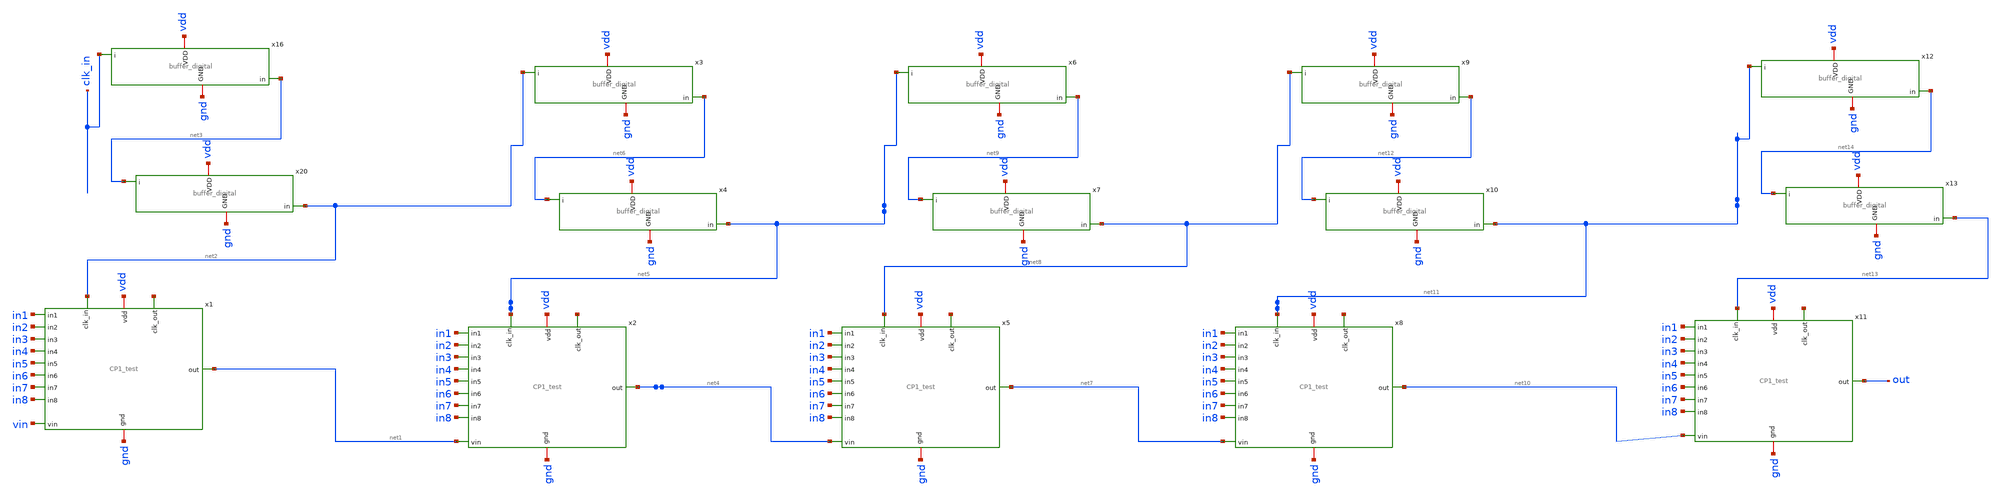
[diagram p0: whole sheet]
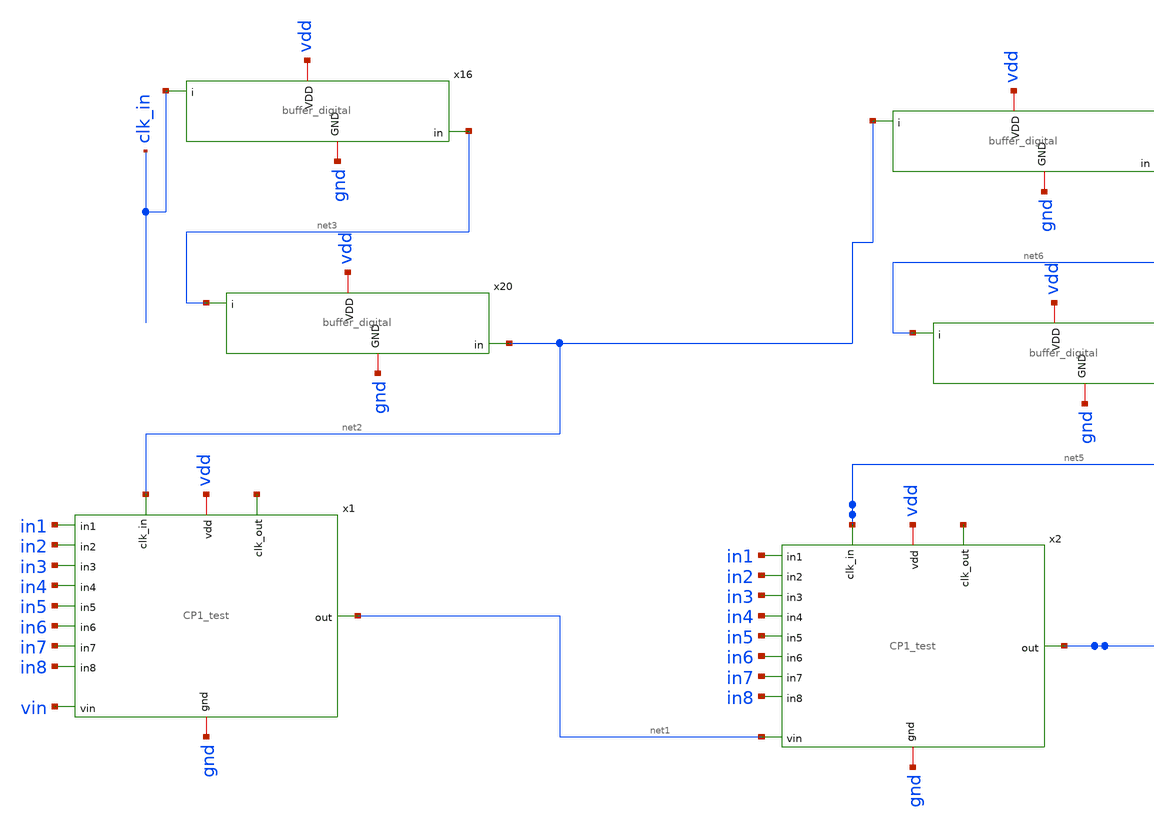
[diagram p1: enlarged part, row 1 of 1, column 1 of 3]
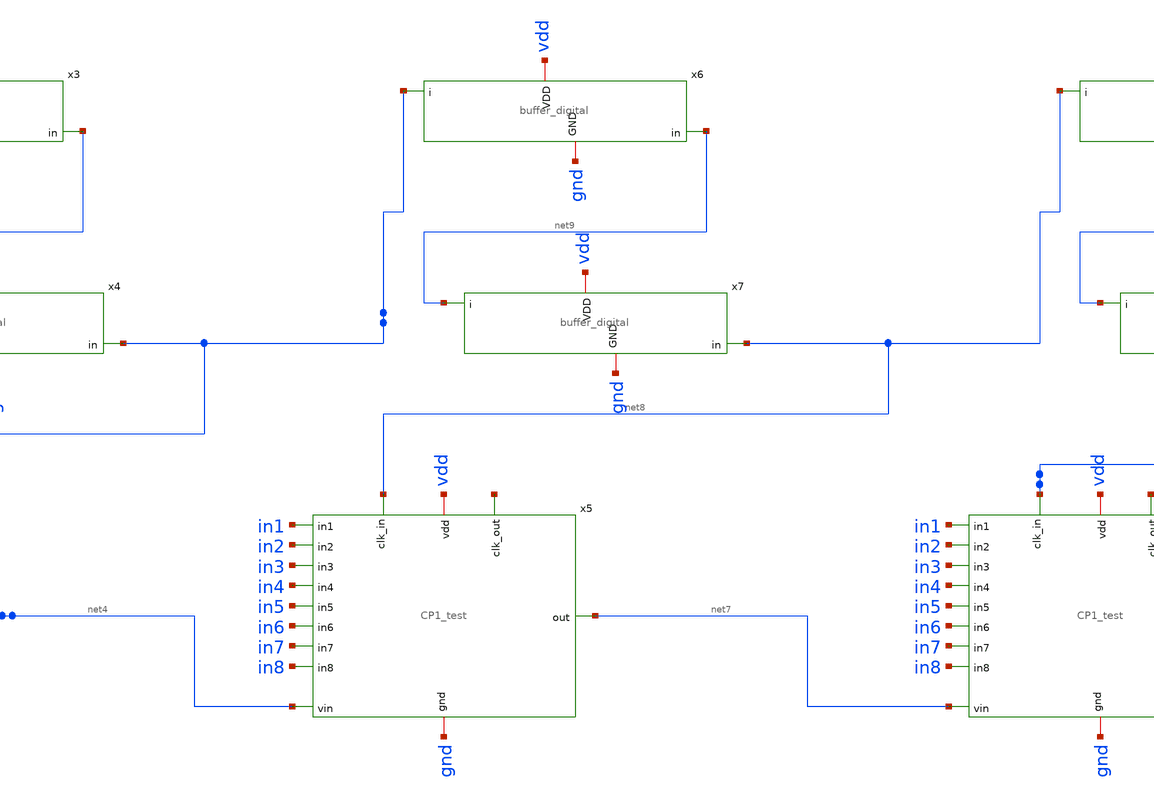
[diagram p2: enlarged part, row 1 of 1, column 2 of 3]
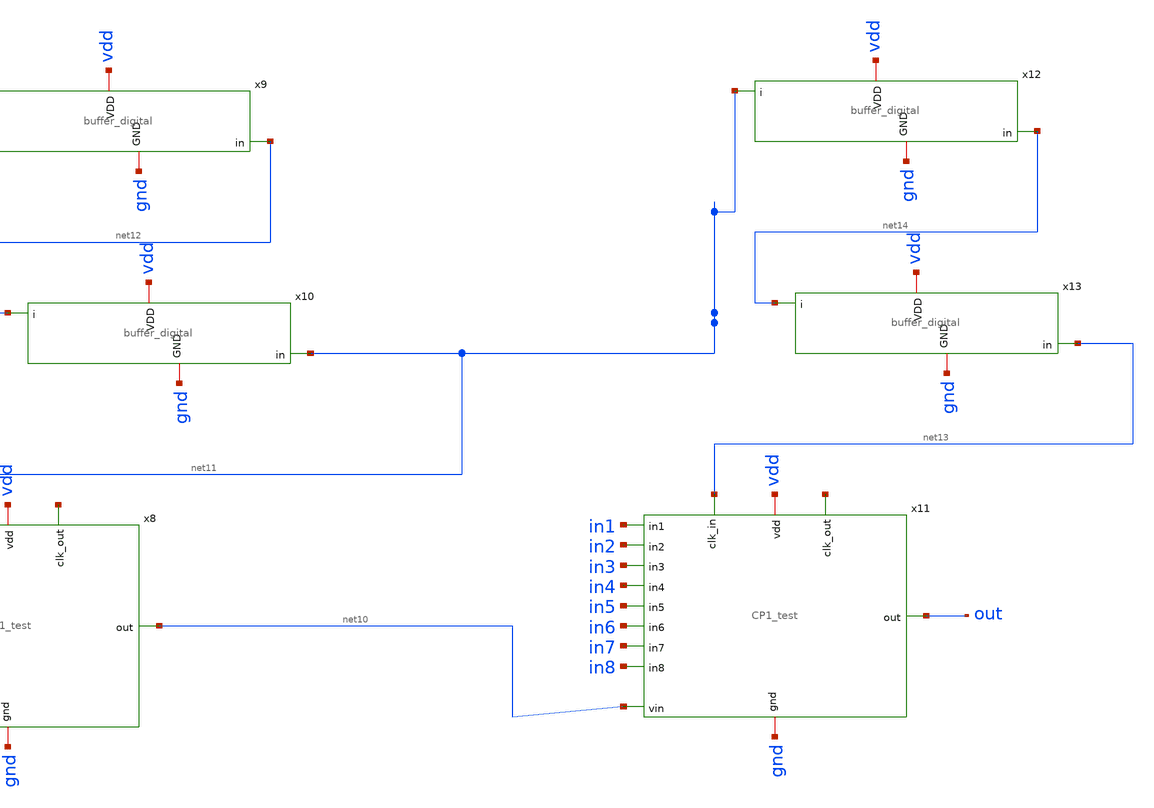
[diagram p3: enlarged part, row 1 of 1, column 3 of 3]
** sch_path: xschem/cp1_buffer_5stage_xschem.sch
**.subckt cp1_buffer_5stage_xschem
x1 gnd net2 vin net1 in1 in2 in3 in4 in5 in6 in7 in8 vdd net15 CP1_test
x16 gnd vdd clk_in net3 buffer_digital
x20 gnd vdd net3 net2 buffer_digital
x2 gnd net5 net1 net4 in1 in2 in3 in4 in5 in6 in7 in8 vdd net16 CP1_test
x3 gnd vdd net2 net6 buffer_digital
x4 gnd vdd net6 net5 buffer_digital
x5 gnd net8 net4 net7 in1 in2 in3 in4 in5 in6 in7 in8 vdd net17 CP1_test
x6 gnd vdd net5 net9 buffer_digital
x7 gnd vdd net9 net8 buffer_digital
x8 gnd net11 net7 net10 in1 in2 in3 in4 in5 in6 in7 in8 vdd net18 CP1_test
x9 gnd vdd net8 net12 buffer_digital
x10 gnd vdd net12 net11 buffer_digital
x11 gnd net13 net10 out in1 in2 in3 in4 in5 in6 in7 in8 vdd net19 CP1_test
x12 gnd vdd net11 net14 buffer_digital
x13 gnd vdd net14 net13 buffer_digital
**.ends
.end
